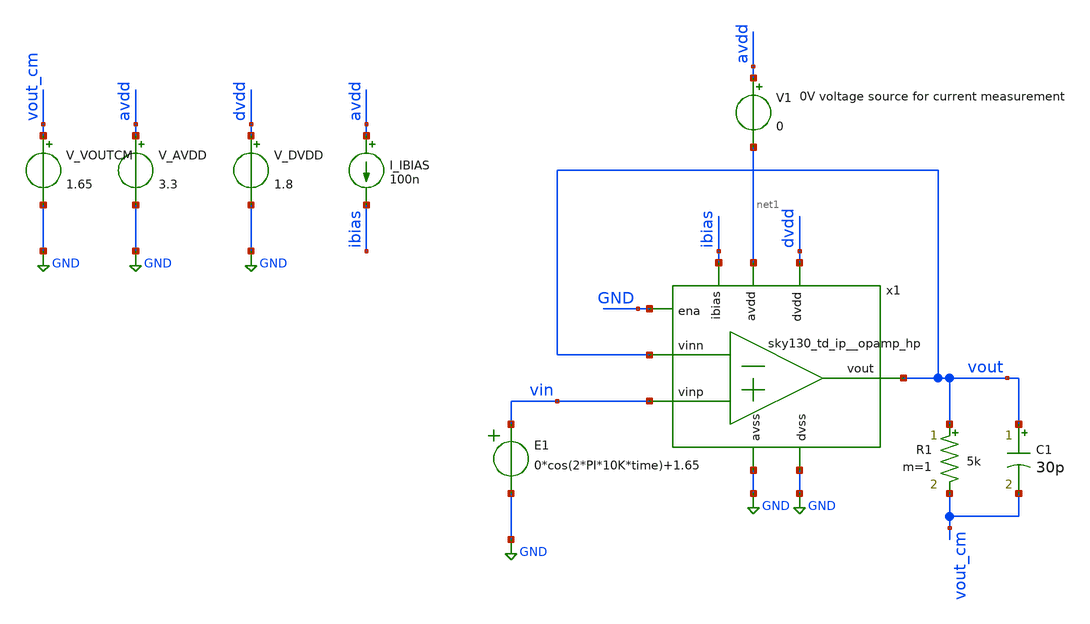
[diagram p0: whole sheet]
** sch_path: xschem/power_disabled.sch
**.subckt power_disabled
x1 net1 vout ibias vout vin GND dvdd GND GND sky130_td_ip__opamp_hp
V_AVDD avdd GND 3.3
.save i(v_avdd)
V_DVDD dvdd GND 1.8
.save i(v_dvdd)
I_IBIAS avdd ibias 100n
R1 vout vout_cm 5k m=1
C1 vout vout_cm 30p m=1
V_VOUTCM vout_cm GND 1.65
.save i(v_voutcm)
E1 vin GND VOL=' 0*cos(2*PI*10K*time)+1.65 '
V1 avdd net1 0
.save i(v1)
**** begin user architecture code


.save all

.control
save all

tran 100n 10u
run

let i_avdd = i(V1)
meas tran max_iavdd MAX i_avdd

echo Max current w/ load: $&max_iavdd

plot i_avdd

.endc




.option TEMP=85
.lib /usr/local/share/pdk/sky130A/libs.tech/combined/sky130.lib.spice ff


**** end user architecture code
**.ends
.GLOBAL GND
.end
